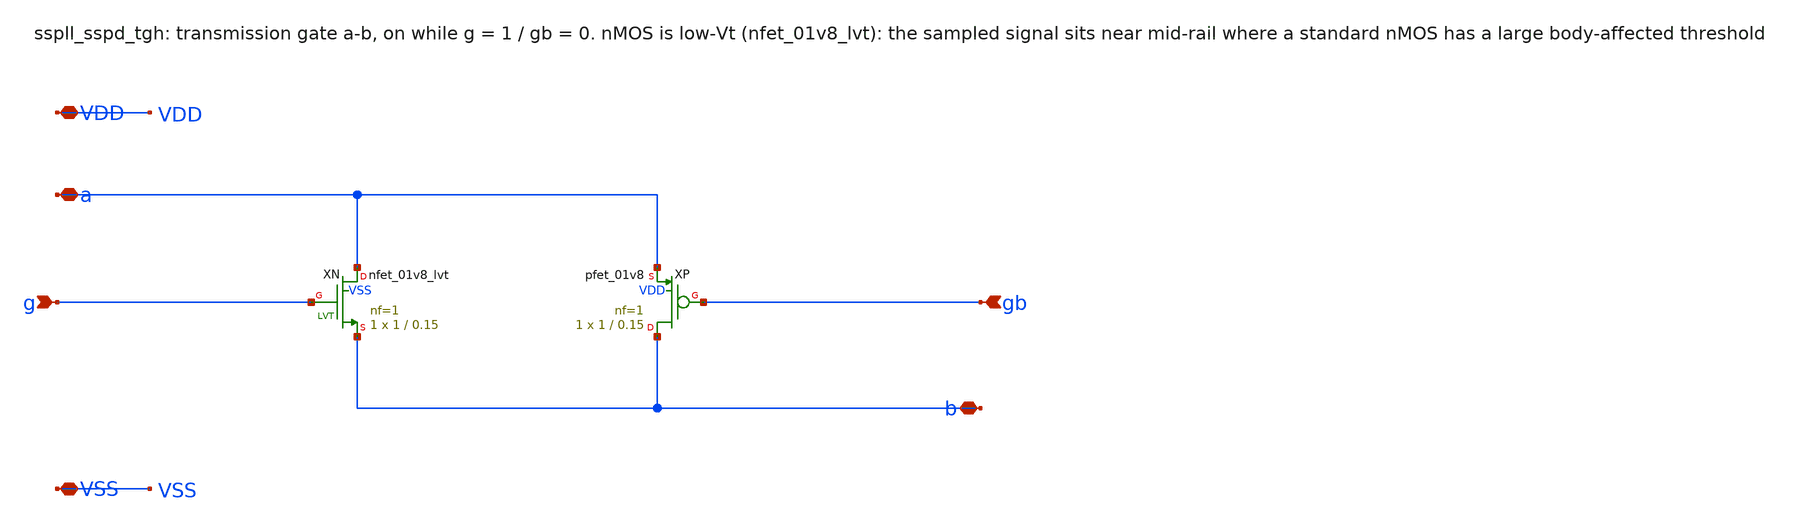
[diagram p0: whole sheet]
** sch_path: xschem/sspd/sspll_sspd_tgh.sch
**.subckt sspll_sspd_tgh a b g gb VDD VSS
*.iopin a
*.iopin b
*.ipin g
*.ipin gb
*.iopin VDD
*.iopin VSS
XXN a g b VSS sky130_fd_pr__nfet_01v8_lvt L=0.15 W=1 nf=1 ad='int((nf+1)/2) * W/nf * 0.29' as='int((nf+2)/2) * W/nf * 0.29'
+ pd='2*int((nf+1)/2) * (W/nf + 0.29)' ps='2*int((nf+2)/2) * (W/nf + 0.29)' nrd='0.29 / W' nrs='0.29 / W'
+ sa=0 sb=0 sd=0 mult=1 m=1
XXP b gb a VDD sky130_fd_pr__pfet_01v8 L=0.15 W=1 nf=1 ad='int((nf+1)/2) * W/nf * 0.29' as='int((nf+2)/2) * W/nf * 0.29'
+ pd='2*int((nf+1)/2) * (W/nf + 0.29)' ps='2*int((nf+2)/2) * (W/nf + 0.29)' nrd='0.29 / W' nrs='0.29 / W'
+ sa=0 sb=0 sd=0 mult=1 m=1
**.ends
.end
